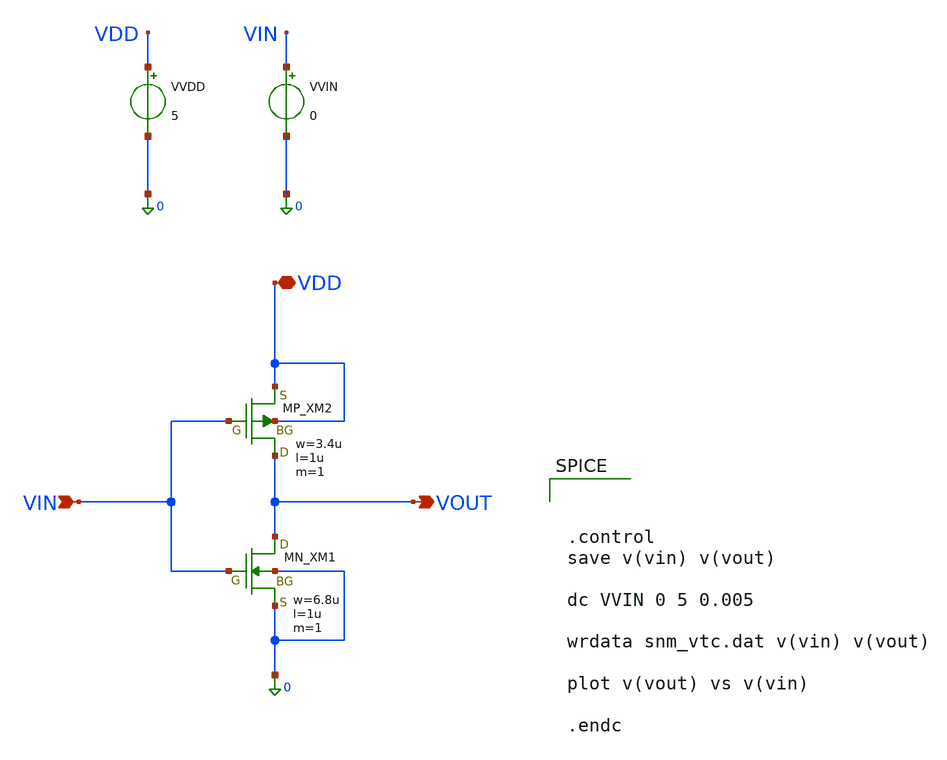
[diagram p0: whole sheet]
** sch_path: cell/snm/tb_snm.sch
**.subckt tb_snm VIN VDD VOUT
*.ipin VIN
*.iopin VDD
*.opin VOUT
XXM1 VOUT VIN 0 0 NMOS w=6.8u l=1u nrd=0 nrs=0 m=1
XXM2 VOUT VIN VDD VDD PMOS w=3.4u l=1u nrd=0 nrs=0 m=1
VVDD VDD 0 5
VVIN VIN 0 0
**** begin user architecture code
 .include $::LIB/ip62_models



.control
save v(vin) v(vout)

dc VVIN 0 5 0.005

wrdata snm_vtc.dat v(vin) v(vout)

plot v(vout) vs v(vin)

.endc


**** end user architecture code
**.ends
.end
